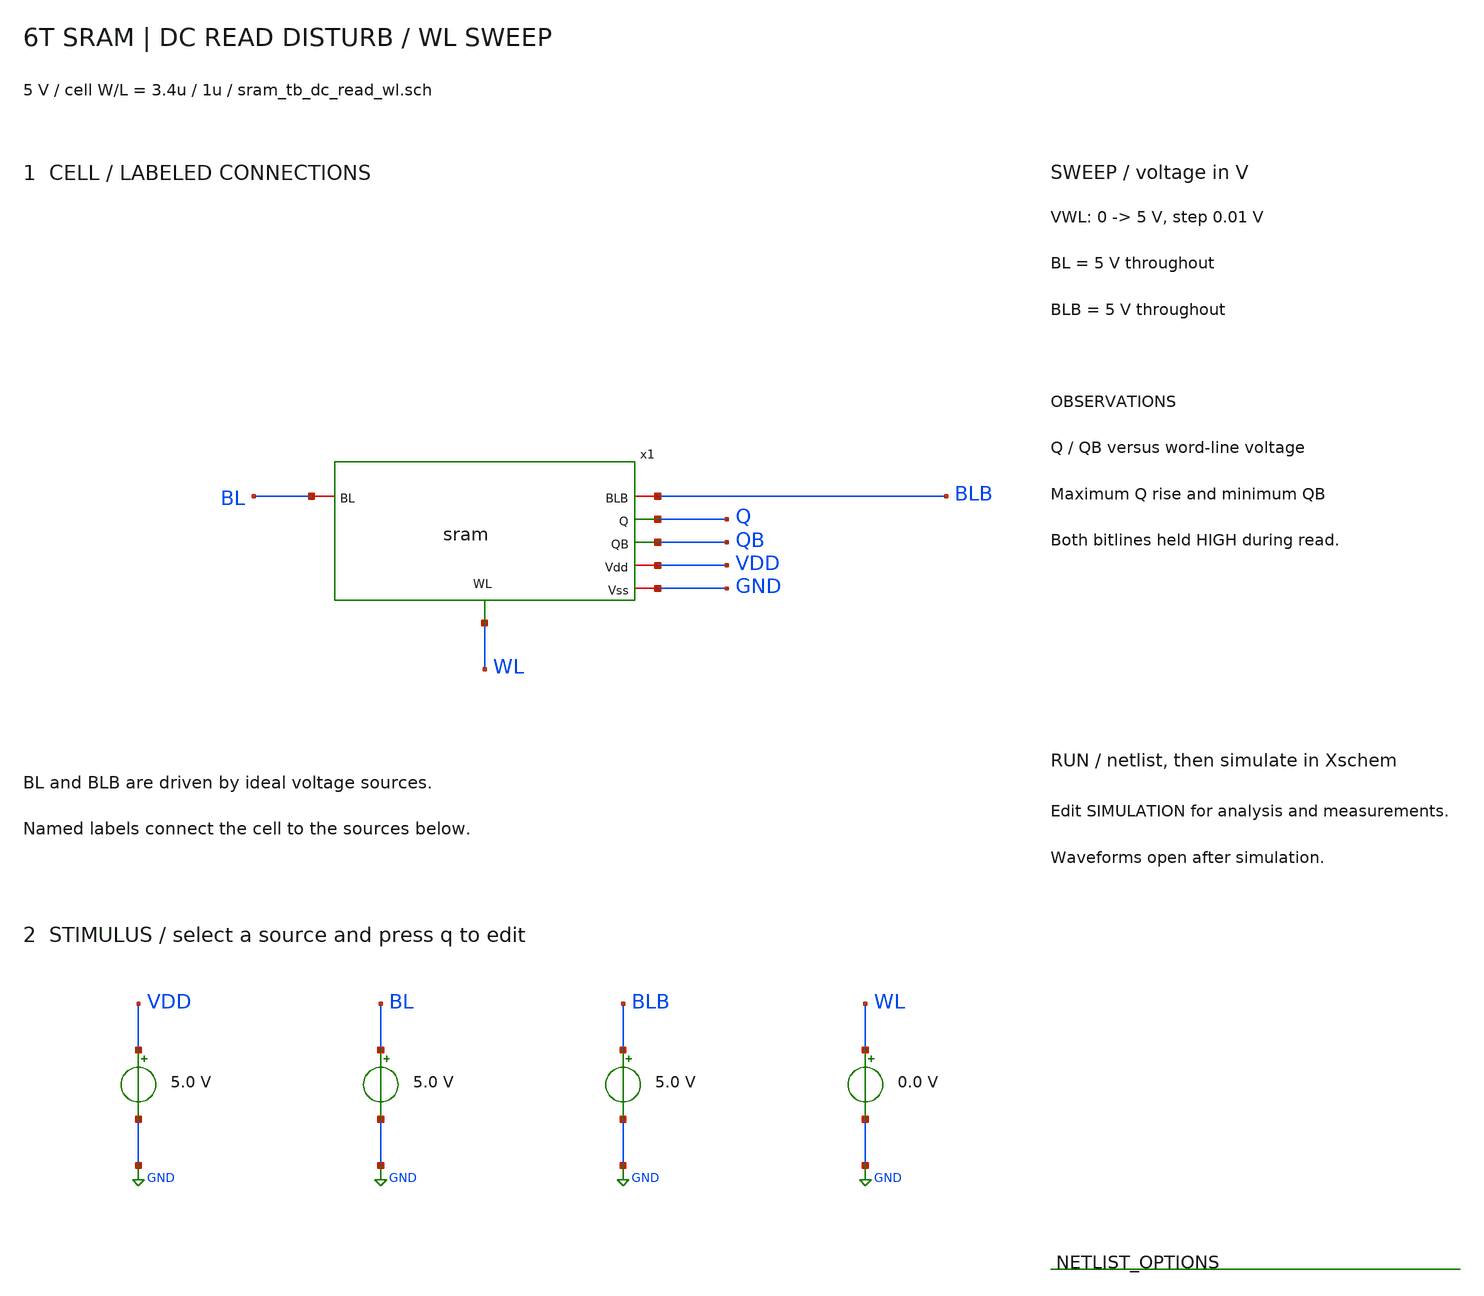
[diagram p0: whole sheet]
** sch_path: member_project/SRAM/PenguinEino/learning/schematics/sram_tb_dc_read_wl.sch
**.subckt sram_tb_dc_read_wl
x1 WL VDD BLB Q QB BL GND sram
Vdd VDD GND 5.0
VBL BL GND 5.0
VBLB BLB GND 5.0
VWL WL GND 0.0
**** begin user architecture code
 .include $::LIB/ip62_models

* DC read-disturb test.
* Both bitlines are held at 5 V (worst-case sustained precharge).
* Follow the stored state Q=0 V, QB=5 V while sweeping WL.
.nodeset v(Q)=0 v(QB)=5

.control
save v(WL) v(Q) v(QB)

dc VWL 0 5 0.01

meas dc Q_DISTURB_MAX max v(Q)
meas dc QB_DROOP_MIN min v(QB)

plot v(Q) v(QB) xlabel 'WL voltage (V)' ylabel 'Storage-node voltage (V)' ylimit -0.2 5.2 title 'DC READ DISTURB: Q=0, QB=5'
.endc

**** end user architecture code
**.ends
.GLOBAL GND
.end
